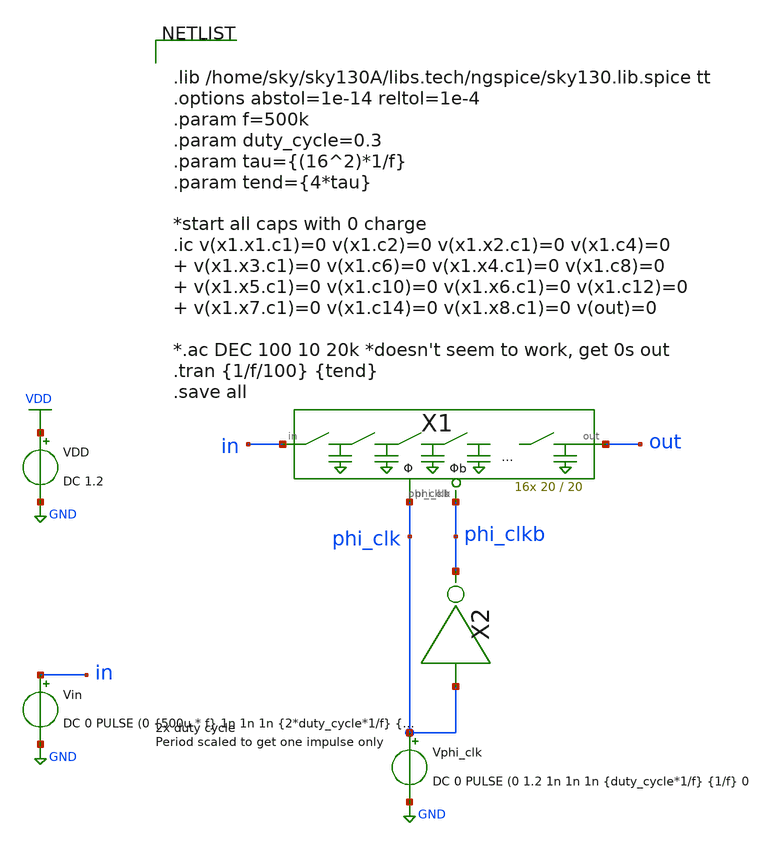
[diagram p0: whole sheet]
** sch_path: xschem/Switched_Caps/16switchcaps_tb_scaled_impulse.sch
**.subckt 16switchcaps_tb_scaled_impulse
Vin in GND DC 0 PULSE (0 {500u * f} 1n 1n 1n {2*duty_cycle*1/f} {tend}
VDD VDD GND DC 1.2
X2 phi_clk phi_clkb inv
Vphi_clk phi_clk GND DC 0 PULSE (0 1.2 1n 1n 1n {duty_cycle*1/f} {1/f} 0
X1 in out phi_clk phi_clkb 16switchcaps W=20 L=20
**** begin user architecture code


.lib /home/sky/sky130A/libs.tech/ngspice/sky130.lib.spice tt
.options abstol=1e-14 reltol=1e-4
.param f=500k
.param duty_cycle=0.3
.param tau={(16^2)*1/f}
.param tend={4*tau}

*start all caps with 0 charge
.ic v(x1.x1.c1)=0 v(x1.c2)=0 v(x1.x2.c1)=0 v(x1.c4)=0   v(x1.x3.c1)=0 v(x1.c6)=0 v(x1.x4.c1)=0
+ v(x1.c8)=0   v(x1.x5.c1)=0 v(x1.c10)=0 v(x1.x6.c1)=0 v(x1.c12)=0   v(x1.x7.c1)=0 v(x1.c14)=0 v(x1.x8.c1)=0
+ v(out)=0

*.ac DEC 100 10 20k *doesn't seem to work, get 0s out
.tran {1/f/100} {tend}
.save all


**** end user architecture code
**.ends

* expanding   symbol:  inv/inv.sym # of pins=2
** sym_path: xschem/inv/inv.sym
** sch_path: xschem/inv/inv.sch
.subckt inv in out
*.ipin in
*.iopin out
XM1 out in GND GND sky130_fd_pr__nfet_01v8 L=0.18 W=0.5 nf=1 ad='int((nf+1)/2) * W/nf * 0.29' as='int((nf+2)/2)
+ * W/nf * 0.29' pd='2*int((nf+1)/2) * (W/nf + 0.29)' ps='2*int((nf+2)/2) * (W/nf + 0.29)' nrd='0.29 /
+ W' nrs='0.29 / W' sa=0 sb=0 sd=0 mult=1 m=1
XM2 out in VDD VDD sky130_fd_pr__pfet_01v8 L=0.18 W=1 nf=1 ad='int((nf+1)/2) * W/nf * 0.29' as='int((nf+2)/2)
+ * W/nf * 0.29' pd='2*int((nf+1)/2) * (W/nf + 0.29)' ps='2*int((nf+2)/2) * (W/nf + 0.29)' nrd='0.29 /
+ W' nrs='0.29 / W' sa=0 sb=0 sd=0 mult=1 m=1
.ends


* expanding   symbol:  Switched_Caps/16switchcaps.sym # of pins=4
** sym_path: xschem/Switched_Caps/16switchcaps.sym
** sch_path: xschem/Switched_Caps/16switchcaps.sch
.subckt 16switchcaps in out phi_clk phi_clkb  W=20 L=20
*.iopin in
*.iopin out
*.ipin phi_clk
*.ipin phi_clkb
X1 in net1 phi_clkb phi_clk phi_clkb phi_clk 2switchcaps W_C=W L_C=L
X2 net1 net2 phi_clkb phi_clk phi_clkb phi_clk 2switchcaps W_C=W L_C=L
X3 net2 net3 phi_clkb phi_clk phi_clkb phi_clk 2switchcaps W_C=W L_C=L
X4 net3 net4 phi_clkb phi_clk phi_clkb phi_clk 2switchcaps W_C=W L_C=L
X5 net4 net5 phi_clkb phi_clk phi_clkb phi_clk 2switchcaps W_C=W L_C=L
X6 net5 net6 phi_clkb phi_clk phi_clkb phi_clk 2switchcaps W_C=W L_C=L
X7 net6 net7 phi_clkb phi_clk phi_clkb phi_clk 2switchcaps W_C=W L_C=L
X8 net7 out phi_clkb phi_clk phi_clkb phi_clk 2switchcaps W_C=W L_C=L
.ends


* expanding   symbol:  Switched_Caps/2switchcaps.sym # of pins=6
** sym_path: xschem/Switched_Caps/2switchcaps.sym
** sch_path: xschem/Switched_Caps/2switchcaps.sch
.subckt 2switchcaps in out phi2_clk_n phi1_clk_n phi1_clk_p phi2_clk_p  Wcap=20 Lcap=20
*.iopin out
*.iopin in
*.ipin phi1_clk_n
*.ipin phi1_clk_p
*.ipin phi2_clk_p
*.ipin phi2_clk_n
XC1 c1 GND sky130_fd_pr__cap_mim_m3_1 W=Wcap L=Lcap MF=1 m=1
X1 in c1 phi1_clk_p phi1_clk_n transmission_gate
X2 c1 out phi2_clk_p phi2_clk_n transmission_gate
XC2 out GND sky130_fd_pr__cap_mim_m3_1 W=Wcap L=Lcap MF=1 m=1
.ends


* expanding   symbol:  transmission_gate/transmission_gate.sym # of pins=4
** sym_path: xschem/transmission_gate/transmission_gate.sym
** sch_path: xschem/transmission_gate/transmission_gate.sch
.subckt transmission_gate in out ctrl_ ctrl
*.iopin in
*.iopin out
*.ipin ctrl_
*.ipin ctrl
XM3 in ctrl out GND sky130_fd_pr__nfet_01v8 L=0.18 W=1 nf=1 ad='int((nf+1)/2) * W/nf * 0.29' as='int((nf+2)/2)
+ * W/nf * 0.29' pd='2*int((nf+1)/2) * (W/nf + 0.29)' ps='2*int((nf+2)/2) * (W/nf + 0.29)' nrd='0.29 /
+ W' nrs='0.29 / W' sa=0 sb=0 sd=0 mult=1 m=1
XM4 out ctrl_ in VDD sky130_fd_pr__pfet_01v8 L=0.18 W=1 nf=1 ad='int((nf+1)/2) * W/nf * 0.29' as='int((nf+2)/2)
+ * W/nf * 0.29' pd='2*int((nf+1)/2) * (W/nf + 0.29)' ps='2*int((nf+2)/2) * (W/nf + 0.29)' nrd='0.29 /
+ W' nrs='0.29 / W' sa=0 sb=0 sd=0 mult=1 m=1
.ends

.GLOBAL GND
.GLOBAL VDD
.end
